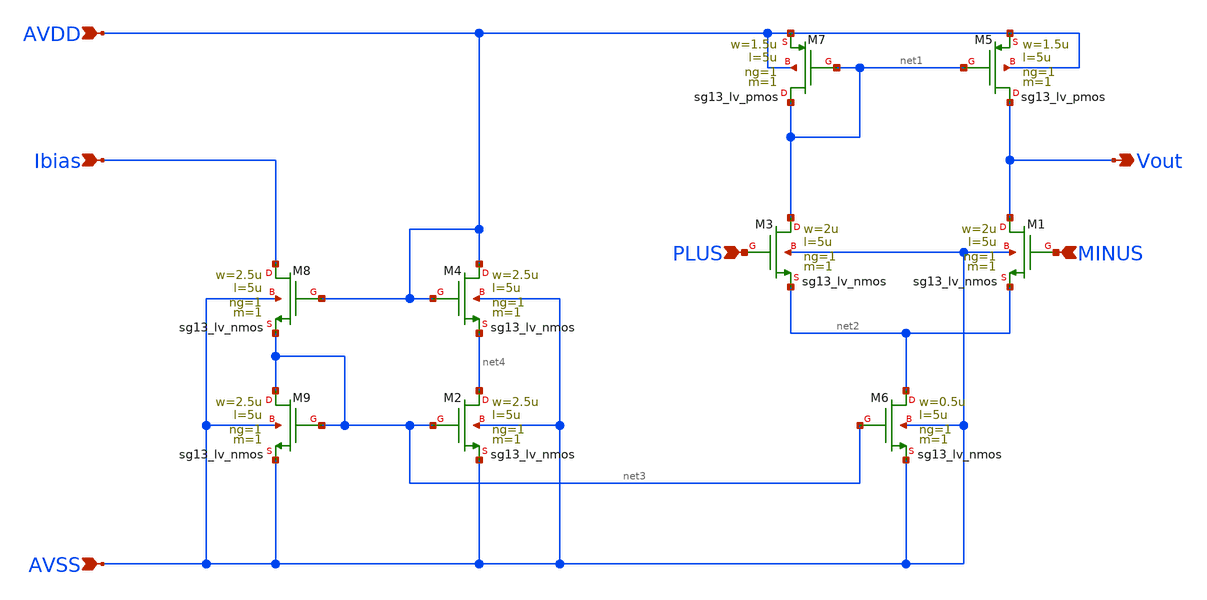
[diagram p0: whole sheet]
** sch_path: Designs/otas/1_schematics/5tota.sch
* (c) 2025 Thesis_HP, Apache-2.0 license
**.subckt 5tota PLUS MINUS Vout AVDD AVSS Ibias
*.ipin PLUS
*.ipin MINUS
*.opin Vout
*.ipin AVDD
*.ipin AVSS
*.ipin Ibias
XM1 Vout MINUS net2 AVSS sg13_lv_nmos w=2u l=5u ng=1 m=1 mm_ok=1
XM3 net1 PLUS net2 AVSS sg13_lv_nmos w=2u l=5u ng=1 m=1 mm_ok=1
XM5 Vout net1 AVDD AVDD sg13_lv_pmos w=1.5u l=5u ng=1 m=1 mm_ok=1
XM7 net1 net1 AVDD AVDD sg13_lv_pmos w=1.5u l=5u ng=1 m=1 mm_ok=1
XM6 net2 net3 AVSS AVSS sg13_lv_nmos w=0.5u l=5u ng=1 m=1 mm_ok=1
XM4 AVDD AVDD net4 AVSS sg13_lv_nmos w=2.5u l=5u ng=1 m=1 mm_ok=1
XM2 net4 net3 AVSS AVSS sg13_lv_nmos w=2.5u l=5u ng=1 m=1 mm_ok=1
XM9 net3 net3 AVSS AVSS sg13_lv_nmos w=2.5u l=5u ng=1 m=1 mm_ok=1
XM8 Ibias AVDD net3 AVSS sg13_lv_nmos w=2.5u l=5u ng=1 m=1 mm_ok=1
**.ends
.end
